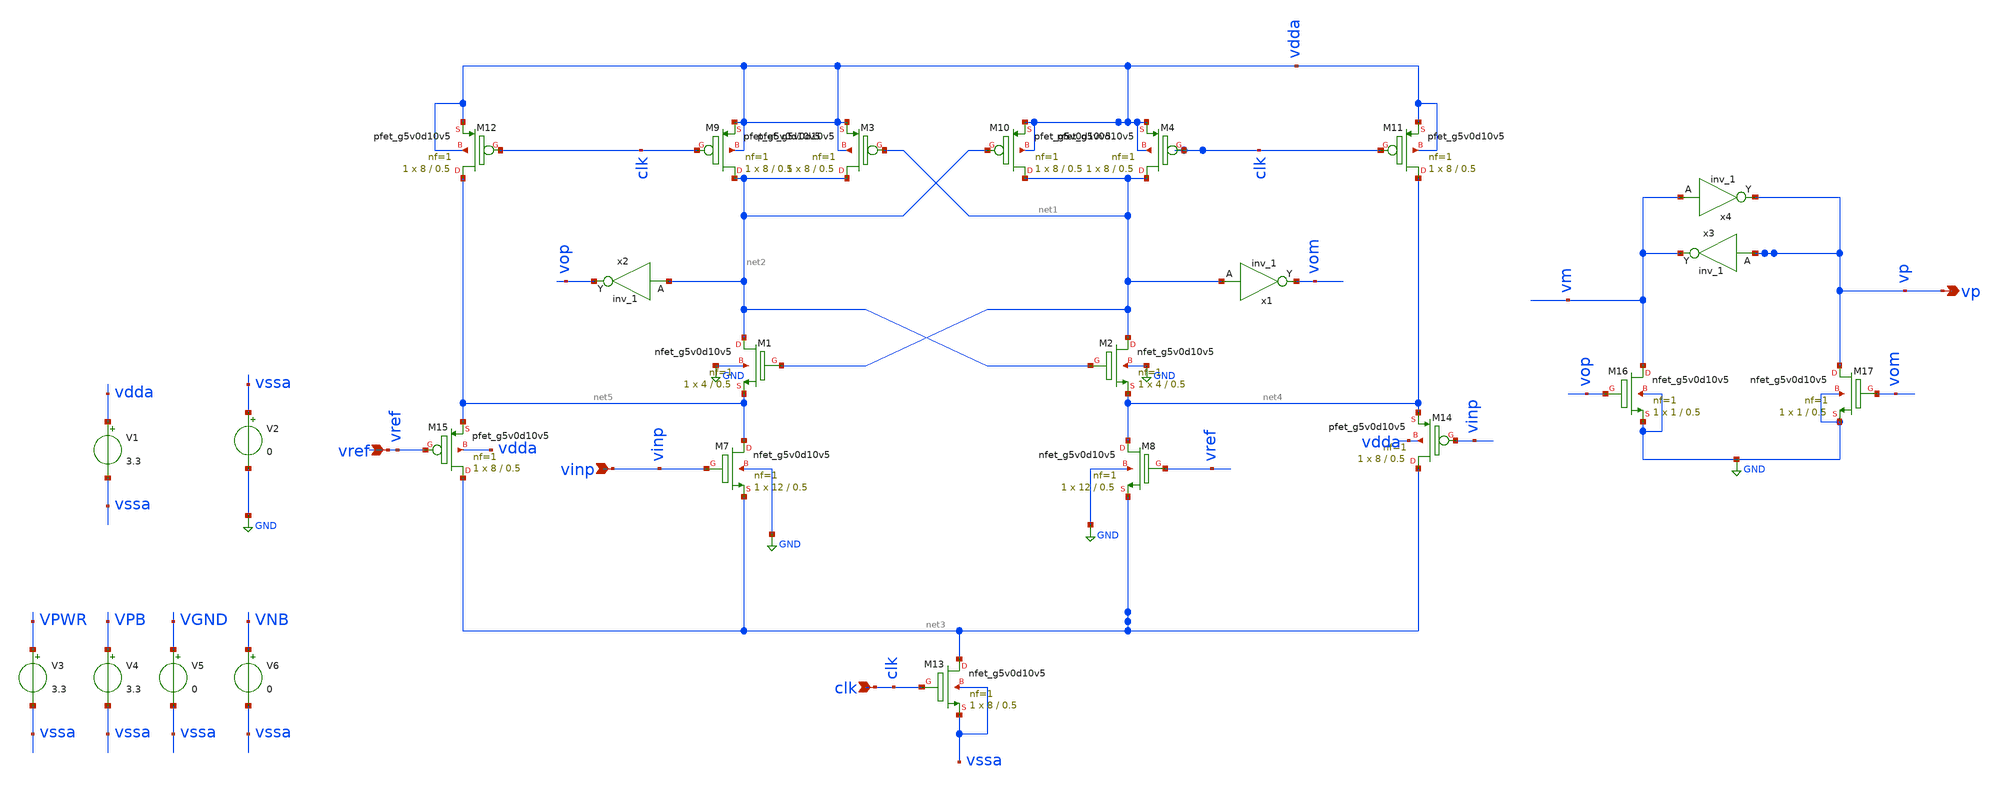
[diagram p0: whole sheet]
** sch_path: xschem/FDC/strongarmlatch.sch
**.subckt strongarmlatch vinp vref clk vp
*.ipin vinp
*.ipin vref
*.ipin clk
*.opin vp
XM7 net5 vinp net3 GND sky130_fd_pr__nfet_g5v0d10v5 L=0.5 W=12 nf=1 ad='int((nf+1)/2) * W/nf * 0.29'
+ as='int((nf+2)/2) * W/nf * 0.29' pd='2*int((nf+1)/2) * (W/nf + 0.29)' ps='2*int((nf+2)/2) * (W/nf + 0.29)'
+ nrd='0.29 / W' nrs='0.29 / W' sa=0 sb=0 sd=0 mult=1 m=1
XM8 net4 vref net3 GND sky130_fd_pr__nfet_g5v0d10v5 L=0.5 W=12 nf=1 ad='int((nf+1)/2) * W/nf * 0.29'
+ as='int((nf+2)/2) * W/nf * 0.29' pd='2*int((nf+1)/2) * (W/nf + 0.29)' ps='2*int((nf+2)/2) * (W/nf + 0.29)'
+ nrd='0.29 / W' nrs='0.29 / W' sa=0 sb=0 sd=0 mult=1 m=1
XM3 net2 net1 vdda vdda sky130_fd_pr__pfet_g5v0d10v5 L=0.5 W=8 nf=1 ad='int((nf+1)/2) * W/nf * 0.29'
+ as='int((nf+2)/2) * W/nf * 0.29' pd='2*int((nf+1)/2) * (W/nf + 0.29)' ps='2*int((nf+2)/2) * (W/nf + 0.29)'
+ nrd='0.29 / W' nrs='0.29 / W' sa=0 sb=0 sd=0 mult=1 m=1
XM9 net2 clk vdda vdda sky130_fd_pr__pfet_g5v0d10v5 L=0.5 W=8 nf=1 ad='int((nf+1)/2) * W/nf * 0.29' as='int((nf+2)/2) * W/nf * 0.29'
+ pd='2*int((nf+1)/2) * (W/nf + 0.29)' ps='2*int((nf+2)/2) * (W/nf + 0.29)' nrd='0.29 / W' nrs='0.29 / W'
+ sa=0 sb=0 sd=0 mult=1 m=1
XM4 net1 clk vdda vdda sky130_fd_pr__pfet_g5v0d10v5 L=0.5 W=8 nf=1 ad='int((nf+1)/2) * W/nf * 0.29' as='int((nf+2)/2) * W/nf * 0.29'
+ pd='2*int((nf+1)/2) * (W/nf + 0.29)' ps='2*int((nf+2)/2) * (W/nf + 0.29)' nrd='0.29 / W' nrs='0.29 / W'
+ sa=0 sb=0 sd=0 mult=1 m=1
XM10 net1 net2 vdda vdda sky130_fd_pr__pfet_g5v0d10v5 L=0.5 W=8 nf=1 ad='int((nf+1)/2) * W/nf * 0.29'
+ as='int((nf+2)/2) * W/nf * 0.29' pd='2*int((nf+1)/2) * (W/nf + 0.29)' ps='2*int((nf+2)/2) * (W/nf + 0.29)'
+ nrd='0.29 / W' nrs='0.29 / W' sa=0 sb=0 sd=0 mult=1 m=1
XM11 net4 clk vdda vdda sky130_fd_pr__pfet_g5v0d10v5 L=0.5 W=8 nf=1 ad='int((nf+1)/2) * W/nf * 0.29'
+ as='int((nf+2)/2) * W/nf * 0.29' pd='2*int((nf+1)/2) * (W/nf + 0.29)' ps='2*int((nf+2)/2) * (W/nf + 0.29)'
+ nrd='0.29 / W' nrs='0.29 / W' sa=0 sb=0 sd=0 mult=1 m=1
XM12 net5 clk vdda vdda sky130_fd_pr__pfet_g5v0d10v5 L=0.5 W=8 nf=1 ad='int((nf+1)/2) * W/nf * 0.29'
+ as='int((nf+2)/2) * W/nf * 0.29' pd='2*int((nf+1)/2) * (W/nf + 0.29)' ps='2*int((nf+2)/2) * (W/nf + 0.29)'
+ nrd='0.29 / W' nrs='0.29 / W' sa=0 sb=0 sd=0 mult=1 m=1
XM13 net3 clk vssa vssa sky130_fd_pr__nfet_g5v0d10v5 L=0.5 W=8 nf=1 ad='int((nf+1)/2) * W/nf * 0.29'
+ as='int((nf+2)/2) * W/nf * 0.29' pd='2*int((nf+1)/2) * (W/nf + 0.29)' ps='2*int((nf+2)/2) * (W/nf + 0.29)'
+ nrd='0.29 / W' nrs='0.29 / W' sa=0 sb=0 sd=0 mult=1 m=1
XM14 net3 vinp net4 vdda sky130_fd_pr__pfet_g5v0d10v5 L=0.5 W=8 nf=1 ad='int((nf+1)/2) * W/nf * 0.29'
+ as='int((nf+2)/2) * W/nf * 0.29' pd='2*int((nf+1)/2) * (W/nf + 0.29)' ps='2*int((nf+2)/2) * (W/nf + 0.29)'
+ nrd='0.29 / W' nrs='0.29 / W' sa=0 sb=0 sd=0 mult=1 m=1
XM15 net3 vref net5 vdda sky130_fd_pr__pfet_g5v0d10v5 L=0.5 W=8 nf=1 ad='int((nf+1)/2) * W/nf * 0.29'
+ as='int((nf+2)/2) * W/nf * 0.29' pd='2*int((nf+1)/2) * (W/nf + 0.29)' ps='2*int((nf+2)/2) * (W/nf + 0.29)'
+ nrd='0.29 / W' nrs='0.29 / W' sa=0 sb=0 sd=0 mult=1 m=1
XM16 vm vop GND GND sky130_fd_pr__nfet_g5v0d10v5 L=0.5 W=1 nf=1 ad='int((nf+1)/2) * W/nf * 0.29' as='int((nf+2)/2) * W/nf * 0.29'
+ pd='2*int((nf+1)/2) * (W/nf + 0.29)' ps='2*int((nf+2)/2) * (W/nf + 0.29)' nrd='0.29 / W' nrs='0.29 / W'
+ sa=0 sb=0 sd=0 mult=1 m=1
XM17 vp vom GND GND sky130_fd_pr__nfet_g5v0d10v5 L=0.5 W=1 nf=1 ad='int((nf+1)/2) * W/nf * 0.29' as='int((nf+2)/2) * W/nf * 0.29'
+ pd='2*int((nf+1)/2) * (W/nf + 0.29)' ps='2*int((nf+2)/2) * (W/nf + 0.29)' nrd='0.29 / W' nrs='0.29 / W'
+ sa=0 sb=0 sd=0 mult=1 m=1
XM1 net2 net1 net5 GND sky130_fd_pr__nfet_g5v0d10v5 L=0.5 W=4 nf=1 ad='int((nf+1)/2) * W/nf * 0.29' as='int((nf+2)/2) * W/nf * 0.29'
+ pd='2*int((nf+1)/2) * (W/nf + 0.29)' ps='2*int((nf+2)/2) * (W/nf + 0.29)' nrd='0.29 / W' nrs='0.29 / W'
+ sa=0 sb=0 sd=0 mult=1 m=1
XM2 net1 net2 net4 GND sky130_fd_pr__nfet_g5v0d10v5 L=0.5 W=4 nf=1 ad='int((nf+1)/2) * W/nf * 0.29' as='int((nf+2)/2) * W/nf * 0.29'
+ pd='2*int((nf+1)/2) * (W/nf + 0.29)' ps='2*int((nf+2)/2) * (W/nf + 0.29)' nrd='0.29 / W' nrs='0.29 / W'
+ sa=0 sb=0 sd=0 mult=1 m=1
x1 net1 VGND VNB VPB VPWR vom sky130_fd_sc_hvl__inv_1
x2 net2 VGND VNB VPB VPWR vop sky130_fd_sc_hvl__inv_1
x4 vm VGND VNB VPB VPWR vp sky130_fd_sc_hvl__inv_1
x3 vp VGND VNB VPB VPWR vm sky130_fd_sc_hvl__inv_1
V1 vdda vssa 3.3
V2 vssa GND 0
V3 VPWR vssa 3.3
V4 VPB vssa 3.3
V5 VGND vssa 0
V6 VNB vssa 0
**.ends
.GLOBAL GND
.end
